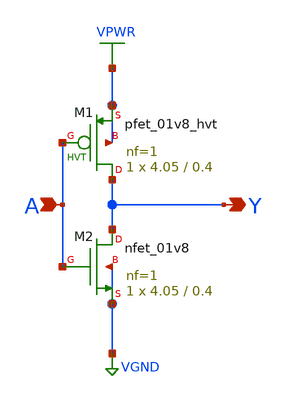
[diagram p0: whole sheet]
** sch_path: xschem/skullfet_inverter.sch
**.subckt skullfet_inverter A Y
*.ipin A
*.opin Y
XM1 Y A VPWR VPWR sky130_fd_pr__pfet_01v8_hvt L=0.4 W=4.05 nf=1 ad=6.2694 as=4.4307 pd=26.64 ps=10.9
+ nrd='0.29 / 4.05 ' nrs='0.29 / 4.05 ' sa=0 sb=0 sd=0 mult=1 m=1
XM2 Y A VGND VGND sky130_fd_pr__nfet_01v8 L=0.4 W=4.05 nf=1 ad=4.2687 as=6.4314 pd=10.82 ps=26.72 nrd='0.29 / 4.05 '
+ nrs='0.29 / 4.05 ' sa=0 sb=0 sd=0 mult=1 m=1
**.ends
.GLOBAL VGND
.GLOBAL VPWR
.end
